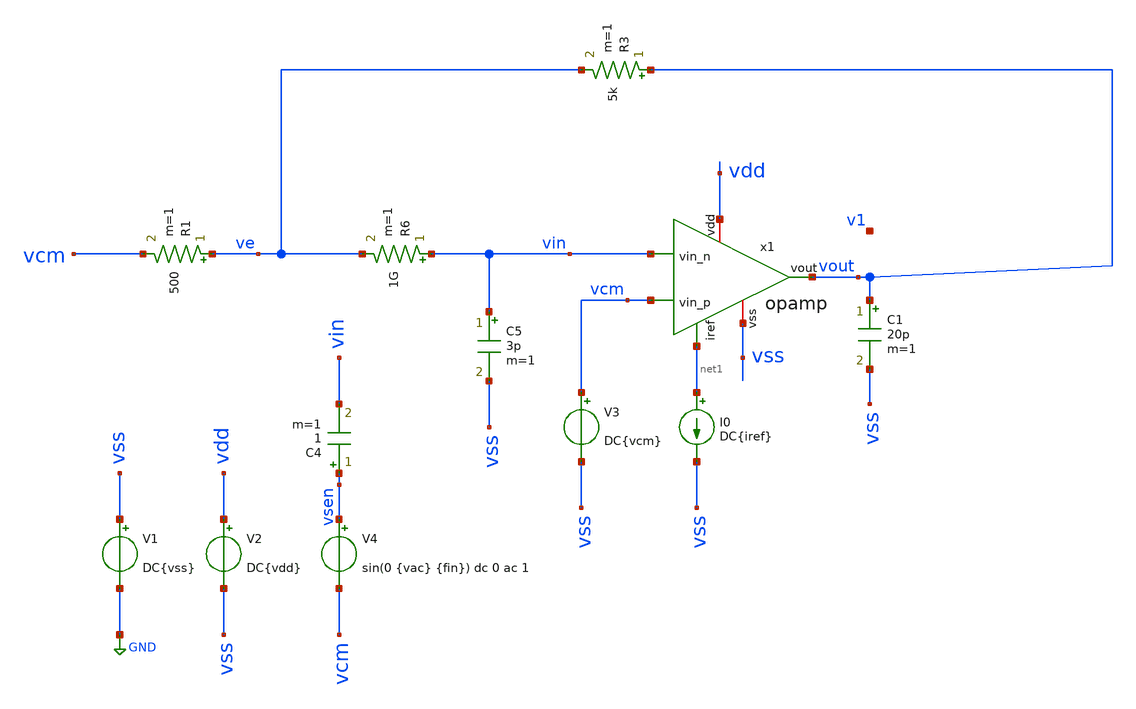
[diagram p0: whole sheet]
** sch_path: opamp/sstb_opamp_openloop.sch
**.subckt sstb_opamp_openloop
V1 vss GND DC{vss}
V2 vdd vss DC{vdd}
V3 vcm vss DC{vcm}
V4 vsen vcm sin(0 {vac} {fin}) dc 0 ac 1
C4 vsen vin 1 m=1
I0 net1 vss DC{iref}
R1 ve vcm 500 m=1
R3 vout ve 5k m=1
C5 vin vss 3p m=1
C1 vout vss 20p m=1
x1 vdd net1 vin vcm vout vss v1 opamp
R6 vin ve 1G m=1
**** begin user architecture code




* Circuit Parameters
.param iref = 95u
.param vdd  = 1.62
.param vss  = 0.0
.param vcm  = 0.72
.param vac  = 60m
.param fin  = 9.765625e5
.options TEMP = 125.0

* Include Models
*.lib ~/skywater/skywater-pdk/libraries/sky130_fd_pr_ngspice/latest/models/corners/sky130.lib TT
.lib /foss/pdks/sky130A/libs.tech/ngspice/sky130.lib.spice ss
*.lib /foss/pdks/sky130A/libs.tech/ngspice/sky130.lib.spice.tt.red tt
* OP Parameters & Singals to save
.save all  @M.X1.XM1.msky130_fd_pr__pfet_01v8_lvt[id] @M.X1.XM1.msky130_fd_pr__pfet_01v8_lvt[vth] @M.X1.XM1.msky130_fd_pr__pfet_01v8_lvt[vgs] @M.X1.XM1.msky130_fd_pr__pfet_01v8_lvt[vds] @M.X1.XM1.msky130_fd_pr__pfet_01v8_lvt[vdsat] @M.X1.XM1.msky130_fd_pr__pfet_01v8_lvt[gm] @M.X1.XM1.msky130_fd_pr__pfet_01v8_lvt[gds]  @M.X1.XM2.msky130_fd_pr__pfet_01v8_lvt[id] @M.X1.XM2.msky130_fd_pr__pfet_01v8_lvt[vth] @M.X1.XM2.msky130_fd_pr__pfet_01v8_lvt[vgs] @M.X1.XM2.msky130_fd_pr__pfet_01v8_lvt[vds] @M.X1.XM2.msky130_fd_pr__pfet_01v8_lvt[vdsat] @M.X1.XM2.msky130_fd_pr__pfet_01v8_lvt[gm] @M.X1.XM2.msky130_fd_pr__pfet_01v8_lvt[gds]  @M.X1.XM3.msky130_fd_pr__nfet_01v8[id] @M.X1.XM3.msky130_fd_pr__nfet_01v8[vth] @M.X1.XM3.msky130_fd_pr__nfet_01v8[vgs] @M.X1.XM3.msky130_fd_pr__nfet_01v8[vds] @M.X1.XM3.msky130_fd_pr__nfet_01v8[vdsat] @M.X1.XM3.msky130_fd_pr__nfet_01v8[gm] @M.X1.XM3.msky130_fd_pr__nfet_01v8[gds]  @M.X1.XM4.msky130_fd_pr__nfet_01v8[id] @M.X1.XM4.msky130_fd_pr__nfet_01v8[vth] @M.X1.XM4.msky130_fd_pr__nfet_01v8[vgs] @M.X1.XM4.msky130_fd_pr__nfet_01v8[vds] @M.X1.XM4.msky130_fd_pr__nfet_01v8[vdsat] @M.X1.XM4.msky130_fd_pr__nfet_01v8[gm] @M.X1.XM4.msky130_fd_pr__nfet_01v8[gds]  @M.X1.XM5.msky130_fd_pr__pfet_01v8[id] @M.X1.XM5.msky130_fd_pr__pfet_01v8[vth] @M.X1.XM5.msky130_fd_pr__pfet_01v8[vgs] @M.X1.XM5.msky130_fd_pr__pfet_01v8[vds] @M.X1.XM5.msky130_fd_pr__pfet_01v8[vdsat] @M.X1.XM5.msky130_fd_pr__pfet_01v8[gm] @M.X1.XM5.msky130_fd_pr__pfet_01v8[gds]  @M.X1.XM6.msky130_fd_pr__nfet_01v8[id] @M.X1.XM6.msky130_fd_pr__nfet_01v8[vth] @M.X1.XM6.msky130_fd_pr__nfet_01v8[vgs] @M.X1.XM6.msky130_fd_pr__nfet_01v8[vds] @M.X1.XM6.msky130_fd_pr__nfet_01v8[vdsat] @M.X1.XM6.msky130_fd_pr__nfet_01v8[gm] @M.X1.XM6.msky130_fd_pr__nfet_01v8[gds]  @M.X1.XM7.msky130_fd_pr__pfet_01v8[id] @M.X1.XM7.msky130_fd_pr__pfet_01v8[vth] @M.X1.XM7.msky130_fd_pr__pfet_01v8[vgs] @M.X1.XM7.msky130_fd_pr__pfet_01v8[vds] @M.X1.XM7.msky130_fd_pr__pfet_01v8[vdsat] @M.X1.XM7.msky130_fd_pr__pfet_01v8[gm] @M.X1.XM7.msky130_fd_pr__pfet_01v8[gds]  @M.X1.XM8.msky130_fd_pr__pfet_01v8[id] @M.X1.XM8.msky130_fd_pr__pfet_01v8[vth] @M.X1.XM8.msky130_fd_pr__pfet_01v8[vgs] @M.X1.XM8.msky130_fd_pr__pfet_01v8[vds] @M.X1.XM8.msky130_fd_pr__pfet_01v8[vdsat] @M.X1.XM8.msky130_fd_pr__pfet_01v8[gm] @M.X1.XM8.msky130_fd_pr__pfet_01v8[gds]  @M.X1.XM9.msky130_fd_pr__nfet_01v8[id] @M.X1.XM9.msky130_fd_pr__nfet_01v8[vth] @M.X1.XM9.msky130_fd_pr__nfet_01v8[vgs] @M.X1.XM9.msky130_fd_pr__nfet_01v8[vds] @M.X1.XM9.msky130_fd_pr__nfet_01v8[vdsat] @M.X1.XM9.msky130_fd_pr__nfet_01v8[gm] @M.X1.XM9.msky130_fd_pr__nfet_01v8[gds]  @M.X9.XM9.msky130_fd_pr__nfet_01v8[gds]

*Simulation
.control
  set color0 = white

  ac dec 100 1 10G
  setplot ac1
  meas ac GBW when vdb(vout)=0
  meas ac DCG find vdb(vout) at=1
  meas ac PM find vp(vout) when vdb(vout)=0
  print PM*180/PI
  meas ac GM find vdb(vout) when vp(vout)=0
  plot vdb(vout) {vp(vout)*180/PI} vdb(v1) {vp(v1)*180/PI}
  write tb_opamp_openloop_ac1.raw

  reset
  op
  setplot op1
  unset filetype
  write tb_opamp_openloop.raw
.endc

.end


**** end user architecture code
**.ends

* expanding   symbol:  opamp.sym # of pins=7
** sym_path: opamp/opamp.sym
** sch_path: opamp/opamp.sch
.subckt opamp vdd iref vin_n vin_p vout vss v1
*.iopin vdd
*.iopin vss
*.ipin vin_n
*.ipin vin_p
*.ipin iref
*.opin vout
*.opin v1
XM5 vp iref vdd vdd sky130_fd_pr__pfet_01v8 L=0.3 W=50 nf=1 ad='W * 0.29' as='W * 0.29' pd='2 * (W + 0.29)'
+ ps='2 * (W + 0.29)' nrd='0.29 / W' nrs='0.29 / W' sa=0 sb=0 sd=0 mult=15 m=15
XM7 vout iref vdd vdd sky130_fd_pr__pfet_01v8 L=0.3 W=50 nf=1 ad='W * 0.29' as='W * 0.29' pd='2 * (W + 0.29)'
+ ps='2 * (W + 0.29)' nrd='0.29 / W' nrs='0.29 / W' sa=0 sb=0 sd=0 mult=24 m=24
XM8 iref iref vdd vdd sky130_fd_pr__pfet_01v8 L=0.3 W=50 nf=1 ad='W * 0.29' as='W * 0.29' pd='2 * (W + 0.29)'
+ ps='2 * (W + 0.29)' nrd='0.29 / W' nrs='0.29 / W' sa=0 sb=0 sd=0 mult=3 m=3
XM1 vbn vin_n vp vp sky130_fd_pr__pfet_01v8_lvt L=0.6 W=86 nf=1 ad='int((nf+1)/2) * W/nf * 0.29' as='int((nf+2)/2) * W/nf * 0.29'
+ pd='2*int((nf+1)/2) * (W/nf + 0.29)' ps='2*int((nf+2)/2) * (W/nf + 0.29)' nrd='0.29 / W' nrs='0.29 / W'
+ sa=0 sb=0 sd=0 mult=10 m=10
XM2 v1 vin_p vp vp sky130_fd_pr__pfet_01v8_lvt L=0.6 W=86 nf=1 ad='int((nf+1)/2) * W/nf * 0.29' as='int((nf+2)/2) * W/nf * 0.29'
+ pd='2*int((nf+1)/2) * (W/nf + 0.29)' ps='2*int((nf+2)/2) * (W/nf + 0.29)' nrd='0.29 / W' nrs='0.29 / W'
+ sa=0 sb=0 sd=0 mult=10 m=10
C1 net2 vout 5.77p m=1
Vmeas net1 vss 0
.save i(vmeas)
XM6 vout v1 net1 net1 sky130_fd_pr__nfet_01v8 L=0.3 W=44 nf=1 ad='W * 0.29' as='W * 0.29' pd='2 * (W + 0.29)'
+ ps='2 * (W + 0.29)' nrd='0.29 / W' nrs='0.29 / W' sa=0 sb=0 sd=0 mult=9 m=9
XM4 v1 vbn net1 net1 sky130_fd_pr__nfet_01v8 L=2.3 W=30 nf=1 ad='W * 0.29' as='W * 0.29' pd='2 * (W + 0.29)'
+ ps='2 * (W + 0.29)' nrd='0.29 / W' nrs='0.29 / W' sa=0 sb=0 sd=0 mult=2 m=2
XM3 vbn vbn net1 net1 sky130_fd_pr__nfet_01v8 L=2.3 W=30 nf=1 ad='W * 0.29' as='W * 0.29' pd='2 * (W + 0.29)'
+ ps='2 * (W + 0.29)' nrd='0.29 / W' nrs='0.29 / W' sa=0 sb=0 sd=0 mult=2 m=2
XM9 net2 vdd v1 vss sky130_fd_pr__nfet_01v8 L=0.38 W=12 nf=1 ad='W * 0.29' as='W * 0.29' pd='2 * (W + 0.29)'
+ ps='2 * (W + 0.29)' nrd='0.29 / W' nrs='0.29 / W' sa=0 sb=0 sd=0 mult=1 m=1
.ends

.GLOBAL GND
.end
